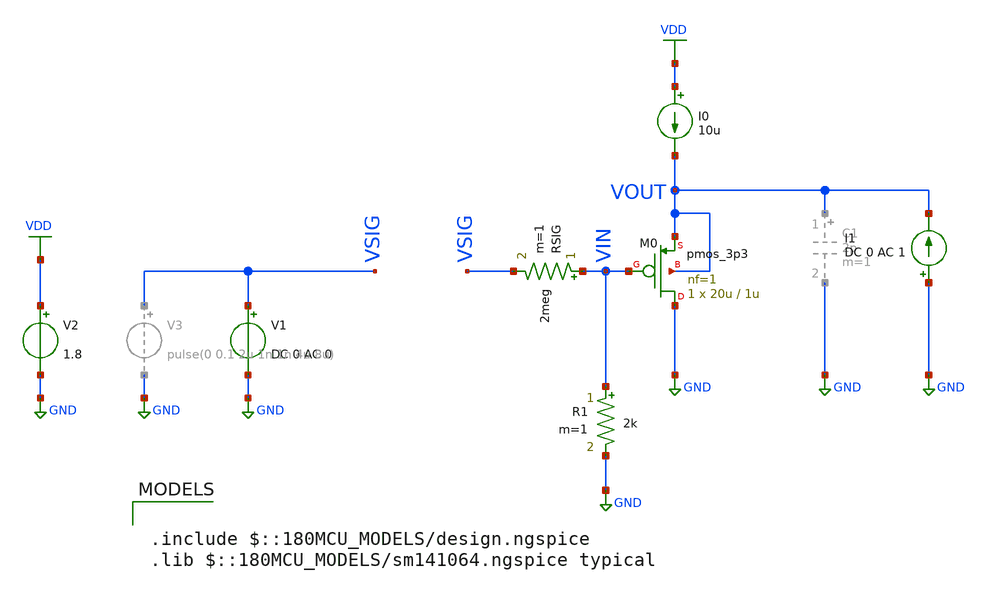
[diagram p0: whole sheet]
** sch_path: ITI_Labs/Lab4/Design/Lab04_compensator.sch
**.subckt Lab04_compensator
V1 VSIG GND DC 0 AC 0
I0 VDD VOUT 10u
V2 VDD GND 1.8
RSIG VIN VSIG 2meg m=1
XM0 GND VIN VOUT VOUT pmos_3p3 L=1u W=20u nf=1 ad='int((nf+1)/2) * W/nf * 0.18u' as='int((nf+2)/2) * W/nf * 0.18u'
+ pd='2*int((nf+1)/2) * (W/nf + 0.18u)' ps='2*int((nf+2)/2) * (W/nf + 0.18u)' nrd='0.18u / W' nrs='0.18u / W'
+ sa=0 sb=0 sd=0 m=1
I1 GND VOUT DC 0 AC 1
R1 VIN GND 2k m=1
**** begin user architecture code

.include $::180MCU_MODELS/design.ngspice
.lib $::180MCU_MODELS/sm141064.ngspice typical



.include sim_script_Comepnsator.sim

**** end user architecture code
**.ends
.GLOBAL GND
.GLOBAL VDD
.end
